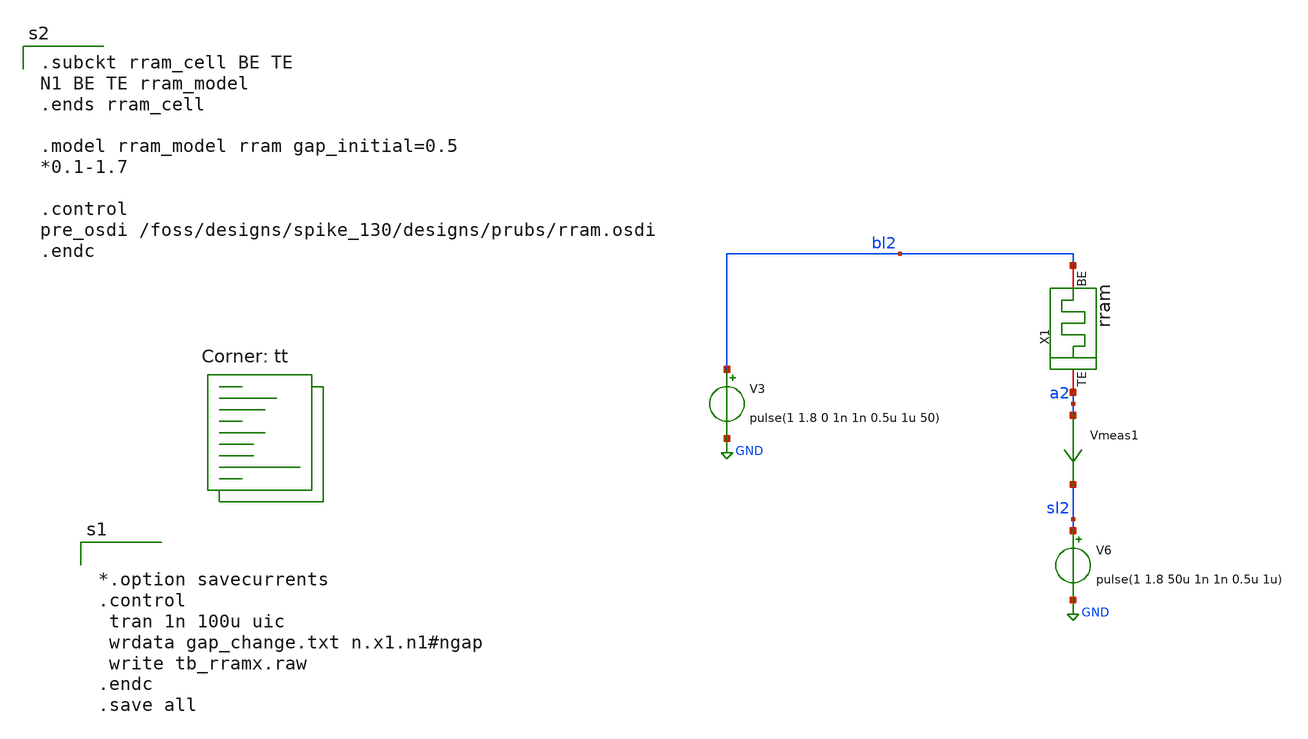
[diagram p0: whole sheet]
** sch_path: designs/prubs/tb_rramx.sch
**.subckt tb_rramx
V3 bl2 GND pulse(1 1.8 0 1n 1n 0.5u 1u 50)
V6 sl2 GND pulse(1 1.8 50u 1n 1n 0.5u 1u)
Vmeas1 a2 sl2 0
.save i(vmeas1)
X1 a2 bl2 rram_cell
**** begin user architecture code
.lib $::SKYWATER_MODELS/sky130.lib.spice tt


*.option savecurrents
.control
 tran 1n 100u uic
 wrdata gap_change.txt n.x1.n1#ngap
 write tb_rramx.raw
.endc
.save all


.subckt rram_cell BE TE
N1 BE TE rram_model
.ends rram_cell

.model rram_model rram gap_initial=0.5
*0.1-1.7

.control
pre_osdi /foss/designs/spike_130/designs/prubs/rram.osdi
.endc

**** end user architecture code
**.ends
.GLOBAL GND
.end
